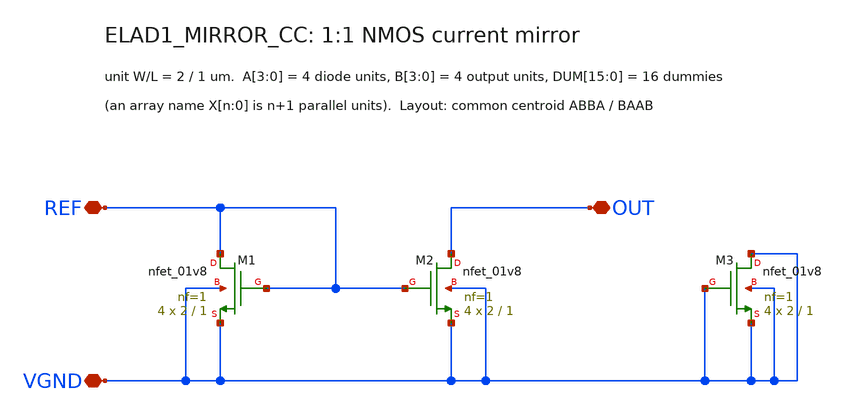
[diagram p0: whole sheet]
** sch_path: cells/ELAD1_MIRROR_CC/schematic/ELAD1_MIRROR_CC.sch
**.subckt ELAD1_MIRROR_CC REF OUT VGND
*.iopin REF
*.iopin OUT
*.iopin VGND
XM1 REF REF VGND VGND sky130_fd_pr__nfet_01v8 L=1 W=2 nf=1 ad='int((1 + 1)/2) * 2 / 1 * 0.29' as='int((1 + 2)/2) * 2 / 1 * 0.29'
+ pd='2*int((1 + 1)/2) * (2 / 1 + 0.29)' ps='2*int((1 + 2)/2) * (2 / 1 + 0.29)' nrd='0.29 / 2 ' nrs='0.29 / 2 '
+ sa=0 sb=0 sd=0 mult=4 m=4
XM2 OUT REF VGND VGND sky130_fd_pr__nfet_01v8 L=1 W=2 nf=1 ad='int((1 + 1)/2) * 2 / 1 * 0.29' as='int((1 + 2)/2) * 2 / 1 * 0.29'
+ pd='2*int((1 + 1)/2) * (2 / 1 + 0.29)' ps='2*int((1 + 2)/2) * (2 / 1 + 0.29)' nrd='0.29 / 2 ' nrs='0.29 / 2 '
+ sa=0 sb=0 sd=0 mult=4 m=4
XM3 VGND VGND VGND VGND sky130_fd_pr__nfet_01v8 L=1 W=2 nf=1 ad='int((1 + 1)/2) * 2 / 1 * 0.29' as='int((1 + 2)/2) * 2 / 1 * 0.29'
+ pd='2*int((1 + 1)/2) * (2 / 1 + 0.29)' ps='2*int((1 + 2)/2) * (2 / 1 + 0.29)' nrd='0.29 / 2 ' nrs='0.29 / 2 '
+ sa=0 sb=0 sd=0 mult=4 m=4
**.ends
.end
